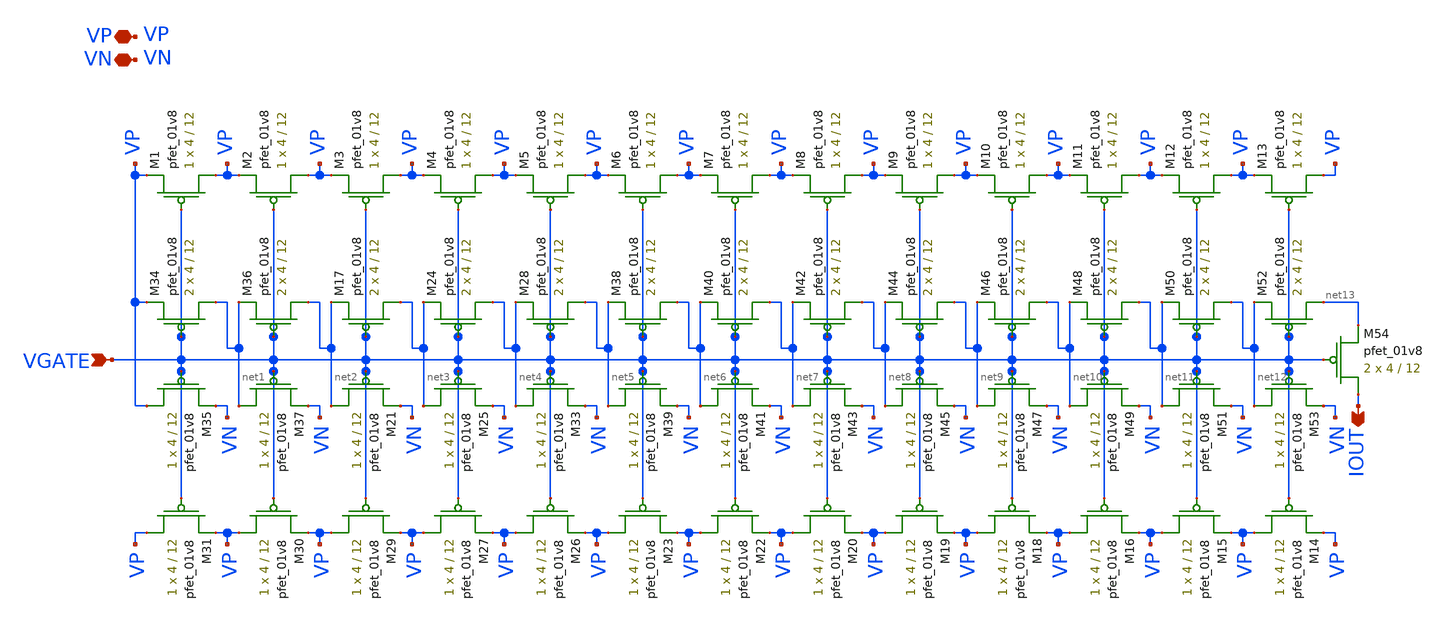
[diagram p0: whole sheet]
** sch_path: dac/layout/current_divider/current_divider_layout.sch
**.subckt current_divider_layout VN IOUT VGATE VP
*.iopin VN
*.opin IOUT
*.ipin VGATE
*.iopin VP
XM34 net1 VGATE VP VP sky130_fd_pr__pfet_01v8 L=12 W=4 nf=1 ad='int((nf+1)/2) * W/nf * 0.29' as='int((nf+2)/2) * W/nf * 0.29'
+ pd='2*int((nf+1)/2) * (W/nf + 0.29)' ps='2*int((nf+2)/2) * (W/nf + 0.29)' nrd='0.29 / W' nrs='0.29 / W'
+ sa=0 sb=0 sd=0 mult=2 m=2
XM35 VP VGATE VN VP sky130_fd_pr__pfet_01v8 L=12 W=4 nf=1 ad='int((nf+1)/2) * W/nf * 0.29' as='int((nf+2)/2) * W/nf * 0.29'
+ pd='2*int((nf+1)/2) * (W/nf + 0.29)' ps='2*int((nf+2)/2) * (W/nf + 0.29)' nrd='0.29 / W' nrs='0.29 / W'
+ sa=0 sb=0 sd=0 mult=1 m=1
XM36 net2 VGATE net1 VP sky130_fd_pr__pfet_01v8 L=12 W=4 nf=1 ad='int((nf+1)/2) * W/nf * 0.29' as='int((nf+2)/2) * W/nf * 0.29'
+ pd='2*int((nf+1)/2) * (W/nf + 0.29)' ps='2*int((nf+2)/2) * (W/nf + 0.29)' nrd='0.29 / W' nrs='0.29 / W'
+ sa=0 sb=0 sd=0 mult=2 m=2
XM37 net1 VGATE VN VP sky130_fd_pr__pfet_01v8 L=12 W=4 nf=1 ad='int((nf+1)/2) * W/nf * 0.29' as='int((nf+2)/2) * W/nf * 0.29'
+ pd='2*int((nf+1)/2) * (W/nf + 0.29)' ps='2*int((nf+2)/2) * (W/nf + 0.29)' nrd='0.29 / W' nrs='0.29 / W'
+ sa=0 sb=0 sd=0 mult=1 m=1
XM17 net3 VGATE net2 VP sky130_fd_pr__pfet_01v8 L=12 W=4 nf=1 ad='int((nf+1)/2) * W/nf * 0.29' as='int((nf+2)/2) * W/nf * 0.29'
+ pd='2*int((nf+1)/2) * (W/nf + 0.29)' ps='2*int((nf+2)/2) * (W/nf + 0.29)' nrd='0.29 / W' nrs='0.29 / W'
+ sa=0 sb=0 sd=0 mult=2 m=2
XM21 net2 VGATE VN VP sky130_fd_pr__pfet_01v8 L=12 W=4 nf=1 ad='int((nf+1)/2) * W/nf * 0.29' as='int((nf+2)/2) * W/nf * 0.29'
+ pd='2*int((nf+1)/2) * (W/nf + 0.29)' ps='2*int((nf+2)/2) * (W/nf + 0.29)' nrd='0.29 / W' nrs='0.29 / W'
+ sa=0 sb=0 sd=0 mult=1 m=1
XM24 net4 VGATE net3 VP sky130_fd_pr__pfet_01v8 L=12 W=4 nf=1 ad='int((nf+1)/2) * W/nf * 0.29' as='int((nf+2)/2) * W/nf * 0.29'
+ pd='2*int((nf+1)/2) * (W/nf + 0.29)' ps='2*int((nf+2)/2) * (W/nf + 0.29)' nrd='0.29 / W' nrs='0.29 / W'
+ sa=0 sb=0 sd=0 mult=2 m=2
XM25 net3 VGATE VN VP sky130_fd_pr__pfet_01v8 L=12 W=4 nf=1 ad='int((nf+1)/2) * W/nf * 0.29' as='int((nf+2)/2) * W/nf * 0.29'
+ pd='2*int((nf+1)/2) * (W/nf + 0.29)' ps='2*int((nf+2)/2) * (W/nf + 0.29)' nrd='0.29 / W' nrs='0.29 / W'
+ sa=0 sb=0 sd=0 mult=1 m=1
XM28 net5 VGATE net4 VP sky130_fd_pr__pfet_01v8 L=12 W=4 nf=1 ad='int((nf+1)/2) * W/nf * 0.29' as='int((nf+2)/2) * W/nf * 0.29'
+ pd='2*int((nf+1)/2) * (W/nf + 0.29)' ps='2*int((nf+2)/2) * (W/nf + 0.29)' nrd='0.29 / W' nrs='0.29 / W'
+ sa=0 sb=0 sd=0 mult=2 m=2
XM33 net4 VGATE VN VP sky130_fd_pr__pfet_01v8 L=12 W=4 nf=1 ad='int((nf+1)/2) * W/nf * 0.29' as='int((nf+2)/2) * W/nf * 0.29'
+ pd='2*int((nf+1)/2) * (W/nf + 0.29)' ps='2*int((nf+2)/2) * (W/nf + 0.29)' nrd='0.29 / W' nrs='0.29 / W'
+ sa=0 sb=0 sd=0 mult=1 m=1
XM38 net6 VGATE net5 VP sky130_fd_pr__pfet_01v8 L=12 W=4 nf=1 ad='int((nf+1)/2) * W/nf * 0.29' as='int((nf+2)/2) * W/nf * 0.29'
+ pd='2*int((nf+1)/2) * (W/nf + 0.29)' ps='2*int((nf+2)/2) * (W/nf + 0.29)' nrd='0.29 / W' nrs='0.29 / W'
+ sa=0 sb=0 sd=0 mult=2 m=2
XM39 net5 VGATE VN VP sky130_fd_pr__pfet_01v8 L=12 W=4 nf=1 ad='int((nf+1)/2) * W/nf * 0.29' as='int((nf+2)/2) * W/nf * 0.29'
+ pd='2*int((nf+1)/2) * (W/nf + 0.29)' ps='2*int((nf+2)/2) * (W/nf + 0.29)' nrd='0.29 / W' nrs='0.29 / W'
+ sa=0 sb=0 sd=0 mult=1 m=1
XM40 net7 VGATE net6 VP sky130_fd_pr__pfet_01v8 L=12 W=4 nf=1 ad='int((nf+1)/2) * W/nf * 0.29' as='int((nf+2)/2) * W/nf * 0.29'
+ pd='2*int((nf+1)/2) * (W/nf + 0.29)' ps='2*int((nf+2)/2) * (W/nf + 0.29)' nrd='0.29 / W' nrs='0.29 / W'
+ sa=0 sb=0 sd=0 mult=2 m=2
XM41 net6 VGATE VN VP sky130_fd_pr__pfet_01v8 L=12 W=4 nf=1 ad='int((nf+1)/2) * W/nf * 0.29' as='int((nf+2)/2) * W/nf * 0.29'
+ pd='2*int((nf+1)/2) * (W/nf + 0.29)' ps='2*int((nf+2)/2) * (W/nf + 0.29)' nrd='0.29 / W' nrs='0.29 / W'
+ sa=0 sb=0 sd=0 mult=1 m=1
XM42 net8 VGATE net7 VP sky130_fd_pr__pfet_01v8 L=12 W=4 nf=1 ad='int((nf+1)/2) * W/nf * 0.29' as='int((nf+2)/2) * W/nf * 0.29'
+ pd='2*int((nf+1)/2) * (W/nf + 0.29)' ps='2*int((nf+2)/2) * (W/nf + 0.29)' nrd='0.29 / W' nrs='0.29 / W'
+ sa=0 sb=0 sd=0 mult=2 m=2
XM43 net7 VGATE VN VP sky130_fd_pr__pfet_01v8 L=12 W=4 nf=1 ad='int((nf+1)/2) * W/nf * 0.29' as='int((nf+2)/2) * W/nf * 0.29'
+ pd='2*int((nf+1)/2) * (W/nf + 0.29)' ps='2*int((nf+2)/2) * (W/nf + 0.29)' nrd='0.29 / W' nrs='0.29 / W'
+ sa=0 sb=0 sd=0 mult=1 m=1
XM44 net9 VGATE net8 VP sky130_fd_pr__pfet_01v8 L=12 W=4 nf=1 ad='int((nf+1)/2) * W/nf * 0.29' as='int((nf+2)/2) * W/nf * 0.29'
+ pd='2*int((nf+1)/2) * (W/nf + 0.29)' ps='2*int((nf+2)/2) * (W/nf + 0.29)' nrd='0.29 / W' nrs='0.29 / W'
+ sa=0 sb=0 sd=0 mult=2 m=2
XM45 net8 VGATE VN VP sky130_fd_pr__pfet_01v8 L=12 W=4 nf=1 ad='int((nf+1)/2) * W/nf * 0.29' as='int((nf+2)/2) * W/nf * 0.29'
+ pd='2*int((nf+1)/2) * (W/nf + 0.29)' ps='2*int((nf+2)/2) * (W/nf + 0.29)' nrd='0.29 / W' nrs='0.29 / W'
+ sa=0 sb=0 sd=0 mult=1 m=1
XM46 net10 VGATE net9 VP sky130_fd_pr__pfet_01v8 L=12 W=4 nf=1 ad='int((nf+1)/2) * W/nf * 0.29' as='int((nf+2)/2) * W/nf * 0.29'
+ pd='2*int((nf+1)/2) * (W/nf + 0.29)' ps='2*int((nf+2)/2) * (W/nf + 0.29)' nrd='0.29 / W' nrs='0.29 / W'
+ sa=0 sb=0 sd=0 mult=2 m=2
XM47 net9 VGATE VN VP sky130_fd_pr__pfet_01v8 L=12 W=4 nf=1 ad='int((nf+1)/2) * W/nf * 0.29' as='int((nf+2)/2) * W/nf * 0.29'
+ pd='2*int((nf+1)/2) * (W/nf + 0.29)' ps='2*int((nf+2)/2) * (W/nf + 0.29)' nrd='0.29 / W' nrs='0.29 / W'
+ sa=0 sb=0 sd=0 mult=1 m=1
XM48 net11 VGATE net10 VP sky130_fd_pr__pfet_01v8 L=12 W=4 nf=1 ad='int((nf+1)/2) * W/nf * 0.29' as='int((nf+2)/2) * W/nf * 0.29'
+ pd='2*int((nf+1)/2) * (W/nf + 0.29)' ps='2*int((nf+2)/2) * (W/nf + 0.29)' nrd='0.29 / W' nrs='0.29 / W'
+ sa=0 sb=0 sd=0 mult=2 m=2
XM49 net10 VGATE VN VP sky130_fd_pr__pfet_01v8 L=12 W=4 nf=1 ad='int((nf+1)/2) * W/nf * 0.29' as='int((nf+2)/2) * W/nf * 0.29'
+ pd='2*int((nf+1)/2) * (W/nf + 0.29)' ps='2*int((nf+2)/2) * (W/nf + 0.29)' nrd='0.29 / W' nrs='0.29 / W'
+ sa=0 sb=0 sd=0 mult=1 m=1
XM50 net12 VGATE net11 VP sky130_fd_pr__pfet_01v8 L=12 W=4 nf=1 ad='int((nf+1)/2) * W/nf * 0.29' as='int((nf+2)/2) * W/nf * 0.29'
+ pd='2*int((nf+1)/2) * (W/nf + 0.29)' ps='2*int((nf+2)/2) * (W/nf + 0.29)' nrd='0.29 / W' nrs='0.29 / W'
+ sa=0 sb=0 sd=0 mult=2 m=2
XM51 net11 VGATE VN VP sky130_fd_pr__pfet_01v8 L=12 W=4 nf=1 ad='int((nf+1)/2) * W/nf * 0.29' as='int((nf+2)/2) * W/nf * 0.29'
+ pd='2*int((nf+1)/2) * (W/nf + 0.29)' ps='2*int((nf+2)/2) * (W/nf + 0.29)' nrd='0.29 / W' nrs='0.29 / W'
+ sa=0 sb=0 sd=0 mult=1 m=1
XM52 net13 VGATE net12 VP sky130_fd_pr__pfet_01v8 L=12 W=4 nf=1 ad='int((nf+1)/2) * W/nf * 0.29' as='int((nf+2)/2) * W/nf * 0.29'
+ pd='2*int((nf+1)/2) * (W/nf + 0.29)' ps='2*int((nf+2)/2) * (W/nf + 0.29)' nrd='0.29 / W' nrs='0.29 / W'
+ sa=0 sb=0 sd=0 mult=2 m=2
XM53 net12 VGATE VN VP sky130_fd_pr__pfet_01v8 L=12 W=4 nf=1 ad='int((nf+1)/2) * W/nf * 0.29' as='int((nf+2)/2) * W/nf * 0.29'
+ pd='2*int((nf+1)/2) * (W/nf + 0.29)' ps='2*int((nf+2)/2) * (W/nf + 0.29)' nrd='0.29 / W' nrs='0.29 / W'
+ sa=0 sb=0 sd=0 mult=1 m=1
XM54 IOUT VGATE net13 VP sky130_fd_pr__pfet_01v8 L=12 W=4 nf=1 ad='int((nf+1)/2) * W/nf * 0.29' as='int((nf+2)/2) * W/nf * 0.29'
+ pd='2*int((nf+1)/2) * (W/nf + 0.29)' ps='2*int((nf+2)/2) * (W/nf + 0.29)' nrd='0.29 / W' nrs='0.29 / W'
+ sa=0 sb=0 sd=0 mult=2 m=2
XM1 VP VGATE VP VP sky130_fd_pr__pfet_01v8 L=12 W=4 nf=1 ad='int((nf+1)/2) * W/nf * 0.29' as='int((nf+2)/2) * W/nf * 0.29'
+ pd='2*int((nf+1)/2) * (W/nf + 0.29)' ps='2*int((nf+2)/2) * (W/nf + 0.29)' nrd='0.29 / W' nrs='0.29 / W'
+ sa=0 sb=0 sd=0 mult=1 m=1
XM2 VP VGATE VP VP sky130_fd_pr__pfet_01v8 L=12 W=4 nf=1 ad='int((nf+1)/2) * W/nf * 0.29' as='int((nf+2)/2) * W/nf * 0.29'
+ pd='2*int((nf+1)/2) * (W/nf + 0.29)' ps='2*int((nf+2)/2) * (W/nf + 0.29)' nrd='0.29 / W' nrs='0.29 / W'
+ sa=0 sb=0 sd=0 mult=1 m=1
XM3 VP VGATE VP VP sky130_fd_pr__pfet_01v8 L=12 W=4 nf=1 ad='int((nf+1)/2) * W/nf * 0.29' as='int((nf+2)/2) * W/nf * 0.29'
+ pd='2*int((nf+1)/2) * (W/nf + 0.29)' ps='2*int((nf+2)/2) * (W/nf + 0.29)' nrd='0.29 / W' nrs='0.29 / W'
+ sa=0 sb=0 sd=0 mult=1 m=1
XM4 VP VGATE VP VP sky130_fd_pr__pfet_01v8 L=12 W=4 nf=1 ad='int((nf+1)/2) * W/nf * 0.29' as='int((nf+2)/2) * W/nf * 0.29'
+ pd='2*int((nf+1)/2) * (W/nf + 0.29)' ps='2*int((nf+2)/2) * (W/nf + 0.29)' nrd='0.29 / W' nrs='0.29 / W'
+ sa=0 sb=0 sd=0 mult=1 m=1
XM5 VP VGATE VP VP sky130_fd_pr__pfet_01v8 L=12 W=4 nf=1 ad='int((nf+1)/2) * W/nf * 0.29' as='int((nf+2)/2) * W/nf * 0.29'
+ pd='2*int((nf+1)/2) * (W/nf + 0.29)' ps='2*int((nf+2)/2) * (W/nf + 0.29)' nrd='0.29 / W' nrs='0.29 / W'
+ sa=0 sb=0 sd=0 mult=1 m=1
XM6 VP VGATE VP VP sky130_fd_pr__pfet_01v8 L=12 W=4 nf=1 ad='int((nf+1)/2) * W/nf * 0.29' as='int((nf+2)/2) * W/nf * 0.29'
+ pd='2*int((nf+1)/2) * (W/nf + 0.29)' ps='2*int((nf+2)/2) * (W/nf + 0.29)' nrd='0.29 / W' nrs='0.29 / W'
+ sa=0 sb=0 sd=0 mult=1 m=1
XM7 VP VGATE VP VP sky130_fd_pr__pfet_01v8 L=12 W=4 nf=1 ad='int((nf+1)/2) * W/nf * 0.29' as='int((nf+2)/2) * W/nf * 0.29'
+ pd='2*int((nf+1)/2) * (W/nf + 0.29)' ps='2*int((nf+2)/2) * (W/nf + 0.29)' nrd='0.29 / W' nrs='0.29 / W'
+ sa=0 sb=0 sd=0 mult=1 m=1
XM8 VP VGATE VP VP sky130_fd_pr__pfet_01v8 L=12 W=4 nf=1 ad='int((nf+1)/2) * W/nf * 0.29' as='int((nf+2)/2) * W/nf * 0.29'
+ pd='2*int((nf+1)/2) * (W/nf + 0.29)' ps='2*int((nf+2)/2) * (W/nf + 0.29)' nrd='0.29 / W' nrs='0.29 / W'
+ sa=0 sb=0 sd=0 mult=1 m=1
XM9 VP VGATE VP VP sky130_fd_pr__pfet_01v8 L=12 W=4 nf=1 ad='int((nf+1)/2) * W/nf * 0.29' as='int((nf+2)/2) * W/nf * 0.29'
+ pd='2*int((nf+1)/2) * (W/nf + 0.29)' ps='2*int((nf+2)/2) * (W/nf + 0.29)' nrd='0.29 / W' nrs='0.29 / W'
+ sa=0 sb=0 sd=0 mult=1 m=1
XM10 VP VGATE VP VP sky130_fd_pr__pfet_01v8 L=12 W=4 nf=1 ad='int((nf+1)/2) * W/nf * 0.29' as='int((nf+2)/2) * W/nf * 0.29'
+ pd='2*int((nf+1)/2) * (W/nf + 0.29)' ps='2*int((nf+2)/2) * (W/nf + 0.29)' nrd='0.29 / W' nrs='0.29 / W'
+ sa=0 sb=0 sd=0 mult=1 m=1
XM11 VP VGATE VP VP sky130_fd_pr__pfet_01v8 L=12 W=4 nf=1 ad='int((nf+1)/2) * W/nf * 0.29' as='int((nf+2)/2) * W/nf * 0.29'
+ pd='2*int((nf+1)/2) * (W/nf + 0.29)' ps='2*int((nf+2)/2) * (W/nf + 0.29)' nrd='0.29 / W' nrs='0.29 / W'
+ sa=0 sb=0 sd=0 mult=1 m=1
XM12 VP VGATE VP VP sky130_fd_pr__pfet_01v8 L=12 W=4 nf=1 ad='int((nf+1)/2) * W/nf * 0.29' as='int((nf+2)/2) * W/nf * 0.29'
+ pd='2*int((nf+1)/2) * (W/nf + 0.29)' ps='2*int((nf+2)/2) * (W/nf + 0.29)' nrd='0.29 / W' nrs='0.29 / W'
+ sa=0 sb=0 sd=0 mult=1 m=1
XM13 VP VGATE VP VP sky130_fd_pr__pfet_01v8 L=12 W=4 nf=1 ad='int((nf+1)/2) * W/nf * 0.29' as='int((nf+2)/2) * W/nf * 0.29'
+ pd='2*int((nf+1)/2) * (W/nf + 0.29)' ps='2*int((nf+2)/2) * (W/nf + 0.29)' nrd='0.29 / W' nrs='0.29 / W'
+ sa=0 sb=0 sd=0 mult=1 m=1
XM14 VP VGATE VP VP sky130_fd_pr__pfet_01v8 L=12 W=4 nf=1 ad='int((nf+1)/2) * W/nf * 0.29' as='int((nf+2)/2) * W/nf * 0.29'
+ pd='2*int((nf+1)/2) * (W/nf + 0.29)' ps='2*int((nf+2)/2) * (W/nf + 0.29)' nrd='0.29 / W' nrs='0.29 / W'
+ sa=0 sb=0 sd=0 mult=1 m=1
XM15 VP VGATE VP VP sky130_fd_pr__pfet_01v8 L=12 W=4 nf=1 ad='int((nf+1)/2) * W/nf * 0.29' as='int((nf+2)/2) * W/nf * 0.29'
+ pd='2*int((nf+1)/2) * (W/nf + 0.29)' ps='2*int((nf+2)/2) * (W/nf + 0.29)' nrd='0.29 / W' nrs='0.29 / W'
+ sa=0 sb=0 sd=0 mult=1 m=1
XM16 VP VGATE VP VP sky130_fd_pr__pfet_01v8 L=12 W=4 nf=1 ad='int((nf+1)/2) * W/nf * 0.29' as='int((nf+2)/2) * W/nf * 0.29'
+ pd='2*int((nf+1)/2) * (W/nf + 0.29)' ps='2*int((nf+2)/2) * (W/nf + 0.29)' nrd='0.29 / W' nrs='0.29 / W'
+ sa=0 sb=0 sd=0 mult=1 m=1
XM18 VP VGATE VP VP sky130_fd_pr__pfet_01v8 L=12 W=4 nf=1 ad='int((nf+1)/2) * W/nf * 0.29' as='int((nf+2)/2) * W/nf * 0.29'
+ pd='2*int((nf+1)/2) * (W/nf + 0.29)' ps='2*int((nf+2)/2) * (W/nf + 0.29)' nrd='0.29 / W' nrs='0.29 / W'
+ sa=0 sb=0 sd=0 mult=1 m=1
XM19 VP VGATE VP VP sky130_fd_pr__pfet_01v8 L=12 W=4 nf=1 ad='int((nf+1)/2) * W/nf * 0.29' as='int((nf+2)/2) * W/nf * 0.29'
+ pd='2*int((nf+1)/2) * (W/nf + 0.29)' ps='2*int((nf+2)/2) * (W/nf + 0.29)' nrd='0.29 / W' nrs='0.29 / W'
+ sa=0 sb=0 sd=0 mult=1 m=1
XM20 VP VGATE VP VP sky130_fd_pr__pfet_01v8 L=12 W=4 nf=1 ad='int((nf+1)/2) * W/nf * 0.29' as='int((nf+2)/2) * W/nf * 0.29'
+ pd='2*int((nf+1)/2) * (W/nf + 0.29)' ps='2*int((nf+2)/2) * (W/nf + 0.29)' nrd='0.29 / W' nrs='0.29 / W'
+ sa=0 sb=0 sd=0 mult=1 m=1
XM22 VP VGATE VP VP sky130_fd_pr__pfet_01v8 L=12 W=4 nf=1 ad='int((nf+1)/2) * W/nf * 0.29' as='int((nf+2)/2) * W/nf * 0.29'
+ pd='2*int((nf+1)/2) * (W/nf + 0.29)' ps='2*int((nf+2)/2) * (W/nf + 0.29)' nrd='0.29 / W' nrs='0.29 / W'
+ sa=0 sb=0 sd=0 mult=1 m=1
XM23 VP VGATE VP VP sky130_fd_pr__pfet_01v8 L=12 W=4 nf=1 ad='int((nf+1)/2) * W/nf * 0.29' as='int((nf+2)/2) * W/nf * 0.29'
+ pd='2*int((nf+1)/2) * (W/nf + 0.29)' ps='2*int((nf+2)/2) * (W/nf + 0.29)' nrd='0.29 / W' nrs='0.29 / W'
+ sa=0 sb=0 sd=0 mult=1 m=1
XM26 VP VGATE VP VP sky130_fd_pr__pfet_01v8 L=12 W=4 nf=1 ad='int((nf+1)/2) * W/nf * 0.29' as='int((nf+2)/2) * W/nf * 0.29'
+ pd='2*int((nf+1)/2) * (W/nf + 0.29)' ps='2*int((nf+2)/2) * (W/nf + 0.29)' nrd='0.29 / W' nrs='0.29 / W'
+ sa=0 sb=0 sd=0 mult=1 m=1
XM27 VP VGATE VP VP sky130_fd_pr__pfet_01v8 L=12 W=4 nf=1 ad='int((nf+1)/2) * W/nf * 0.29' as='int((nf+2)/2) * W/nf * 0.29'
+ pd='2*int((nf+1)/2) * (W/nf + 0.29)' ps='2*int((nf+2)/2) * (W/nf + 0.29)' nrd='0.29 / W' nrs='0.29 / W'
+ sa=0 sb=0 sd=0 mult=1 m=1
XM29 VP VGATE VP VP sky130_fd_pr__pfet_01v8 L=12 W=4 nf=1 ad='int((nf+1)/2) * W/nf * 0.29' as='int((nf+2)/2) * W/nf * 0.29'
+ pd='2*int((nf+1)/2) * (W/nf + 0.29)' ps='2*int((nf+2)/2) * (W/nf + 0.29)' nrd='0.29 / W' nrs='0.29 / W'
+ sa=0 sb=0 sd=0 mult=1 m=1
XM30 VP VGATE VP VP sky130_fd_pr__pfet_01v8 L=12 W=4 nf=1 ad='int((nf+1)/2) * W/nf * 0.29' as='int((nf+2)/2) * W/nf * 0.29'
+ pd='2*int((nf+1)/2) * (W/nf + 0.29)' ps='2*int((nf+2)/2) * (W/nf + 0.29)' nrd='0.29 / W' nrs='0.29 / W'
+ sa=0 sb=0 sd=0 mult=1 m=1
XM31 VP VGATE VP VP sky130_fd_pr__pfet_01v8 L=12 W=4 nf=1 ad='int((nf+1)/2) * W/nf * 0.29' as='int((nf+2)/2) * W/nf * 0.29'
+ pd='2*int((nf+1)/2) * (W/nf + 0.29)' ps='2*int((nf+2)/2) * (W/nf + 0.29)' nrd='0.29 / W' nrs='0.29 / W'
+ sa=0 sb=0 sd=0 mult=1 m=1
**.ends
.end
